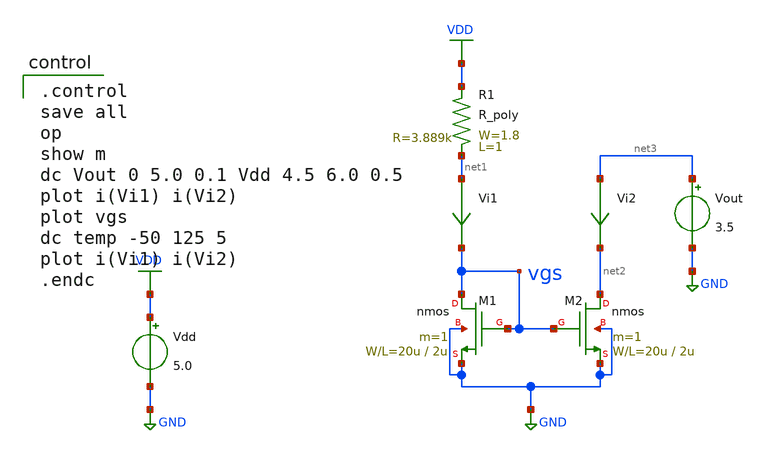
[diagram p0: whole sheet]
** sch_path: OR1/PTC06/current-source/cs-basic.sch
**.subckt cs-basic
Vdd VDD GND 5.0
Vi1 net1 vgs 0
.save i(vi1)
Vi2 net3 net2 0
.save i(vi2)
Vout net3 GND 3.5
R1 net1 VDD R_poly W=1.8 L=1
M1 vgs vgs GND GND nmos L=2u W=20u m=1
M2 net2 vgs GND GND nmos L=2u W=20u m=1
**** begin user architecture code

.control
save all
op
show m
dc Vout 0 5.0 0.1 Vdd 4.5 6.0 0.5
plot i(Vi1) i(Vi2)
plot vgs
dc temp -50 125 5
plot i(Vi1) i(Vi2)
.endc

 .include $::LIB/mos.lib
.include $::LIB/passive.lib
.include $::LIB/diode.lib
**** end user architecture code
**.ends
.GLOBAL GND
.GLOBAL VDD
.end
